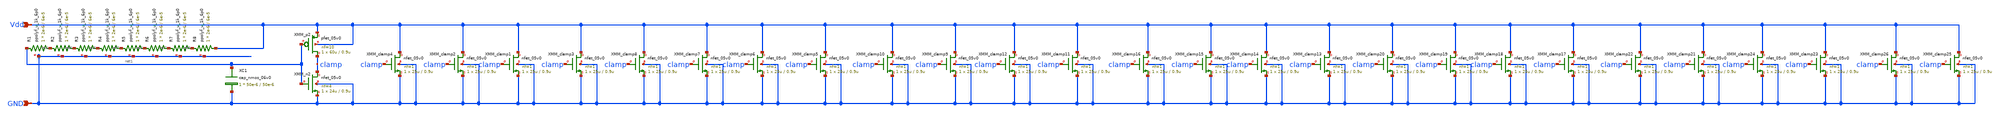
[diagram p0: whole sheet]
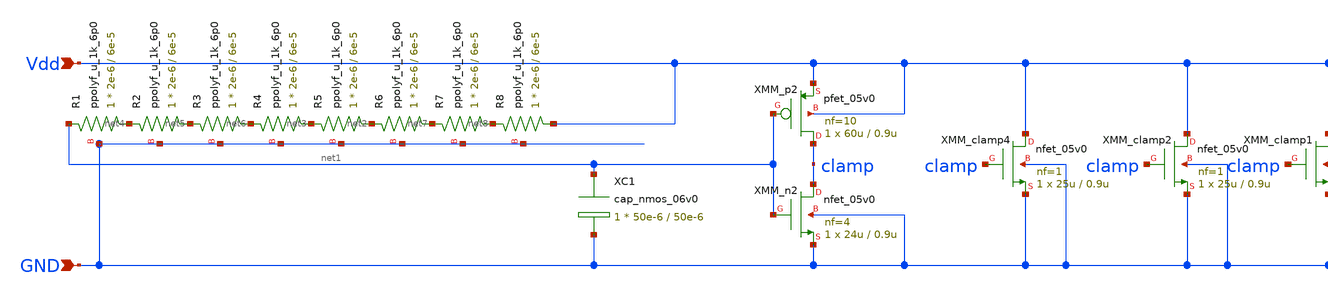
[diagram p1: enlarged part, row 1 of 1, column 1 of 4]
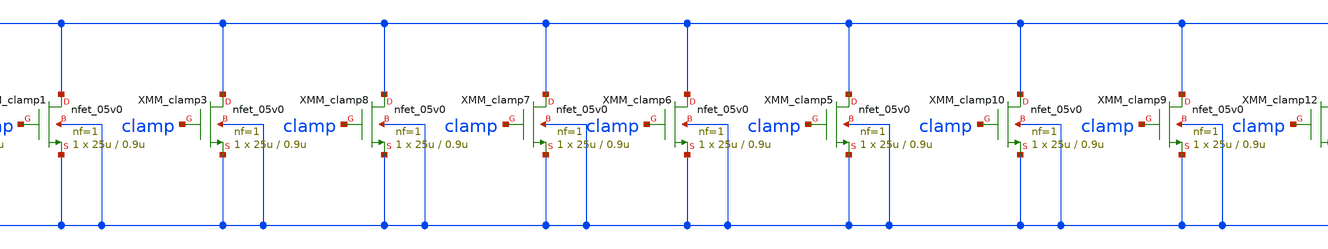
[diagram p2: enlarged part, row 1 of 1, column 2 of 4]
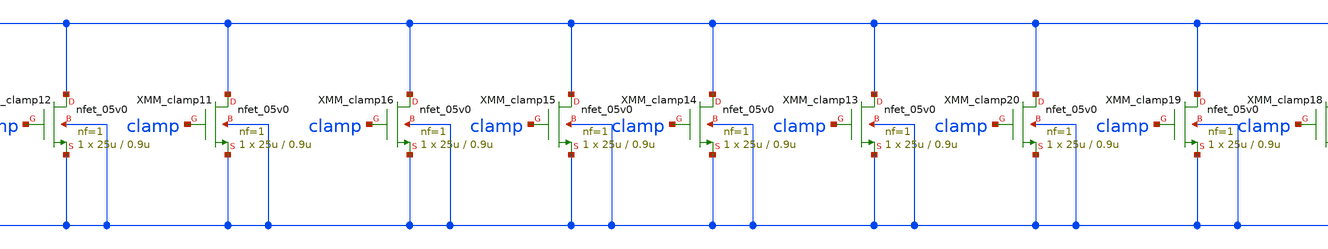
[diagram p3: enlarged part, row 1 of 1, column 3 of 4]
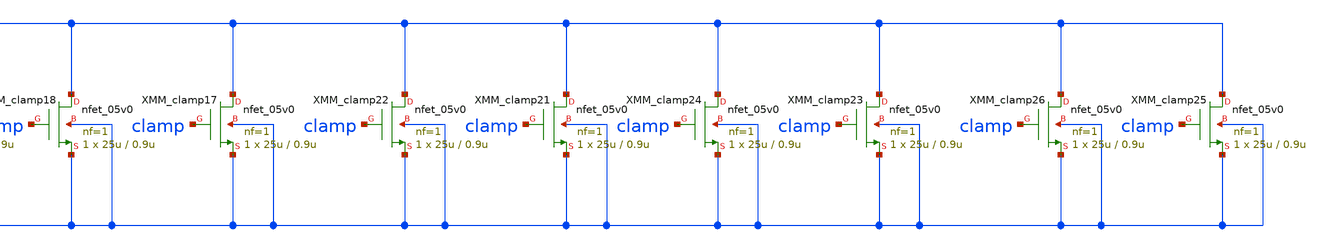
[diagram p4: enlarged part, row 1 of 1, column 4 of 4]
** sch_path: MG_ESD_protection/MG_power_clamp_ESD.sch
**.subckt MG_power_clamp_ESD Vdd GND
*.ipin Vdd
*.ipin GND
XC1 net1 GND cap_nmos_06v0 c_width=50e-6 c_length=50e-6 m=1
XMM_clamp3 Vdd clamp GND GND nfet_05v0 L=0.9u W=25u nf=1 ad='int((nf+1)/2) * W/nf * 0.18u' as='int((nf+2)/2) * W/nf * 0.18u'
+ pd='2*int((nf+1)/2) * (W/nf + 0.18u)' ps='2*int((nf+2)/2) * (W/nf + 0.18u)' nrd='0.18u / W' nrs='0.18u / W'
+ sa=0 sb=0 sd=0 m=1
XMM_clamp1 Vdd clamp GND GND nfet_05v0 L=0.9u W=25u nf=1 ad='int((nf+1)/2) * W/nf * 0.18u' as='int((nf+2)/2) * W/nf * 0.18u'
+ pd='2*int((nf+1)/2) * (W/nf + 0.18u)' ps='2*int((nf+2)/2) * (W/nf + 0.18u)' nrd='0.18u / W' nrs='0.18u / W'
+ sa=0 sb=0 sd=0 m=1
XMM_clamp2 Vdd clamp GND GND nfet_05v0 L=0.9u W=25u nf=1 ad='int((nf+1)/2) * W/nf * 0.18u' as='int((nf+2)/2) * W/nf * 0.18u'
+ pd='2*int((nf+1)/2) * (W/nf + 0.18u)' ps='2*int((nf+2)/2) * (W/nf + 0.18u)' nrd='0.18u / W' nrs='0.18u / W'
+ sa=0 sb=0 sd=0 m=1
XMM_clamp4 Vdd clamp GND GND nfet_05v0 L=0.9u W=25u nf=1 ad='int((nf+1)/2) * W/nf * 0.18u' as='int((nf+2)/2) * W/nf * 0.18u'
+ pd='2*int((nf+1)/2) * (W/nf + 0.18u)' ps='2*int((nf+2)/2) * (W/nf + 0.18u)' nrd='0.18u / W' nrs='0.18u / W'
+ sa=0 sb=0 sd=0 m=1
XMM_clamp5 Vdd clamp GND GND nfet_05v0 L=0.9u W=25u nf=1 ad='int((nf+1)/2) * W/nf * 0.18u' as='int((nf+2)/2) * W/nf * 0.18u'
+ pd='2*int((nf+1)/2) * (W/nf + 0.18u)' ps='2*int((nf+2)/2) * (W/nf + 0.18u)' nrd='0.18u / W' nrs='0.18u / W'
+ sa=0 sb=0 sd=0 m=1
XMM_clamp6 Vdd clamp GND GND nfet_05v0 L=0.9u W=25u nf=1 ad='int((nf+1)/2) * W/nf * 0.18u' as='int((nf+2)/2) * W/nf * 0.18u'
+ pd='2*int((nf+1)/2) * (W/nf + 0.18u)' ps='2*int((nf+2)/2) * (W/nf + 0.18u)' nrd='0.18u / W' nrs='0.18u / W'
+ sa=0 sb=0 sd=0 m=1
XMM_clamp7 Vdd clamp GND GND nfet_05v0 L=0.9u W=25u nf=1 ad='int((nf+1)/2) * W/nf * 0.18u' as='int((nf+2)/2) * W/nf * 0.18u'
+ pd='2*int((nf+1)/2) * (W/nf + 0.18u)' ps='2*int((nf+2)/2) * (W/nf + 0.18u)' nrd='0.18u / W' nrs='0.18u / W'
+ sa=0 sb=0 sd=0 m=1
XMM_clamp8 Vdd clamp GND GND nfet_05v0 L=0.9u W=25u nf=1 ad='int((nf+1)/2) * W/nf * 0.18u' as='int((nf+2)/2) * W/nf * 0.18u'
+ pd='2*int((nf+1)/2) * (W/nf + 0.18u)' ps='2*int((nf+2)/2) * (W/nf + 0.18u)' nrd='0.18u / W' nrs='0.18u / W'
+ sa=0 sb=0 sd=0 m=1
XMM_clamp9 Vdd clamp GND GND nfet_05v0 L=0.9u W=25u nf=1 ad='int((nf+1)/2) * W/nf * 0.18u' as='int((nf+2)/2) * W/nf * 0.18u'
+ pd='2*int((nf+1)/2) * (W/nf + 0.18u)' ps='2*int((nf+2)/2) * (W/nf + 0.18u)' nrd='0.18u / W' nrs='0.18u / W'
+ sa=0 sb=0 sd=0 m=1
XMM_clamp10 Vdd clamp GND GND nfet_05v0 L=0.9u W=25u nf=1 ad='int((nf+1)/2) * W/nf * 0.18u' as='int((nf+2)/2) * W/nf * 0.18u'
+ pd='2*int((nf+1)/2) * (W/nf + 0.18u)' ps='2*int((nf+2)/2) * (W/nf + 0.18u)' nrd='0.18u / W' nrs='0.18u / W'
+ sa=0 sb=0 sd=0 m=1
XMM_clamp11 Vdd clamp GND GND nfet_05v0 L=0.9u W=25u nf=1 ad='int((nf+1)/2) * W/nf * 0.18u' as='int((nf+2)/2) * W/nf * 0.18u'
+ pd='2*int((nf+1)/2) * (W/nf + 0.18u)' ps='2*int((nf+2)/2) * (W/nf + 0.18u)' nrd='0.18u / W' nrs='0.18u / W'
+ sa=0 sb=0 sd=0 m=1
XMM_clamp12 Vdd clamp GND GND nfet_05v0 L=0.9u W=25u nf=1 ad='int((nf+1)/2) * W/nf * 0.18u' as='int((nf+2)/2) * W/nf * 0.18u'
+ pd='2*int((nf+1)/2) * (W/nf + 0.18u)' ps='2*int((nf+2)/2) * (W/nf + 0.18u)' nrd='0.18u / W' nrs='0.18u / W'
+ sa=0 sb=0 sd=0 m=1
XR5 net2 net3 GND ppolyf_u_1k_6p0 r_width=2e-6 r_length=6e-5 m=1
XMM_clamp13 Vdd clamp GND GND nfet_05v0 L=0.9u W=25u nf=1 ad='int((nf+1)/2) * W/nf * 0.18u' as='int((nf+2)/2) * W/nf * 0.18u'
+ pd='2*int((nf+1)/2) * (W/nf + 0.18u)' ps='2*int((nf+2)/2) * (W/nf + 0.18u)' nrd='0.18u / W' nrs='0.18u / W'
+ sa=0 sb=0 sd=0 m=1
XMM_clamp14 Vdd clamp GND GND nfet_05v0 L=0.9u W=25u nf=1 ad='int((nf+1)/2) * W/nf * 0.18u' as='int((nf+2)/2) * W/nf * 0.18u'
+ pd='2*int((nf+1)/2) * (W/nf + 0.18u)' ps='2*int((nf+2)/2) * (W/nf + 0.18u)' nrd='0.18u / W' nrs='0.18u / W'
+ sa=0 sb=0 sd=0 m=1
XMM_clamp15 Vdd clamp GND GND nfet_05v0 L=0.9u W=25u nf=1 ad='int((nf+1)/2) * W/nf * 0.18u' as='int((nf+2)/2) * W/nf * 0.18u'
+ pd='2*int((nf+1)/2) * (W/nf + 0.18u)' ps='2*int((nf+2)/2) * (W/nf + 0.18u)' nrd='0.18u / W' nrs='0.18u / W'
+ sa=0 sb=0 sd=0 m=1
XMM_clamp16 Vdd clamp GND GND nfet_05v0 L=0.9u W=25u nf=1 ad='int((nf+1)/2) * W/nf * 0.18u' as='int((nf+2)/2) * W/nf * 0.18u'
+ pd='2*int((nf+1)/2) * (W/nf + 0.18u)' ps='2*int((nf+2)/2) * (W/nf + 0.18u)' nrd='0.18u / W' nrs='0.18u / W'
+ sa=0 sb=0 sd=0 m=1
XMM_clamp17 Vdd clamp GND GND nfet_05v0 L=0.9u W=25u nf=1 ad='int((nf+1)/2) * W/nf * 0.18u' as='int((nf+2)/2) * W/nf * 0.18u'
+ pd='2*int((nf+1)/2) * (W/nf + 0.18u)' ps='2*int((nf+2)/2) * (W/nf + 0.18u)' nrd='0.18u / W' nrs='0.18u / W'
+ sa=0 sb=0 sd=0 m=1
XMM_clamp18 Vdd clamp GND GND nfet_05v0 L=0.9u W=25u nf=1 ad='int((nf+1)/2) * W/nf * 0.18u' as='int((nf+2)/2) * W/nf * 0.18u'
+ pd='2*int((nf+1)/2) * (W/nf + 0.18u)' ps='2*int((nf+2)/2) * (W/nf + 0.18u)' nrd='0.18u / W' nrs='0.18u / W'
+ sa=0 sb=0 sd=0 m=1
XMM_clamp19 Vdd clamp GND GND nfet_05v0 L=0.9u W=25u nf=1 ad='int((nf+1)/2) * W/nf * 0.18u' as='int((nf+2)/2) * W/nf * 0.18u'
+ pd='2*int((nf+1)/2) * (W/nf + 0.18u)' ps='2*int((nf+2)/2) * (W/nf + 0.18u)' nrd='0.18u / W' nrs='0.18u / W'
+ sa=0 sb=0 sd=0 m=1
XMM_clamp20 Vdd clamp GND GND nfet_05v0 L=0.9u W=25u nf=1 ad='int((nf+1)/2) * W/nf * 0.18u' as='int((nf+2)/2) * W/nf * 0.18u'
+ pd='2*int((nf+1)/2) * (W/nf + 0.18u)' ps='2*int((nf+2)/2) * (W/nf + 0.18u)' nrd='0.18u / W' nrs='0.18u / W'
+ sa=0 sb=0 sd=0 m=1
XMM_clamp21 Vdd clamp GND GND nfet_05v0 L=0.9u W=25u nf=1 ad='int((nf+1)/2) * W/nf * 0.18u' as='int((nf+2)/2) * W/nf * 0.18u'
+ pd='2*int((nf+1)/2) * (W/nf + 0.18u)' ps='2*int((nf+2)/2) * (W/nf + 0.18u)' nrd='0.18u / W' nrs='0.18u / W'
+ sa=0 sb=0 sd=0 m=1
XMM_clamp22 Vdd clamp GND GND nfet_05v0 L=0.9u W=25u nf=1 ad='int((nf+1)/2) * W/nf * 0.18u' as='int((nf+2)/2) * W/nf * 0.18u'
+ pd='2*int((nf+1)/2) * (W/nf + 0.18u)' ps='2*int((nf+2)/2) * (W/nf + 0.18u)' nrd='0.18u / W' nrs='0.18u / W'
+ sa=0 sb=0 sd=0 m=1
XMM_clamp23 Vdd clamp GND GND nfet_05v0 L=0.9u W=25u nf=1 ad='int((nf+1)/2) * W/nf * 0.18u' as='int((nf+2)/2) * W/nf * 0.18u'
+ pd='2*int((nf+1)/2) * (W/nf + 0.18u)' ps='2*int((nf+2)/2) * (W/nf + 0.18u)' nrd='0.18u / W' nrs='0.18u / W'
+ sa=0 sb=0 sd=0 m=1
XMM_clamp24 Vdd clamp GND GND nfet_05v0 L=0.9u W=25u nf=1 ad='int((nf+1)/2) * W/nf * 0.18u' as='int((nf+2)/2) * W/nf * 0.18u'
+ pd='2*int((nf+1)/2) * (W/nf + 0.18u)' ps='2*int((nf+2)/2) * (W/nf + 0.18u)' nrd='0.18u / W' nrs='0.18u / W'
+ sa=0 sb=0 sd=0 m=1
XMM_p2 clamp net1 Vdd Vdd pfet_05v0 L=0.9u W=60u nf=10 ad='int((nf+1)/2) * W/nf * 0.18u' as='int((nf+2)/2) * W/nf * 0.18u'
+ pd='2*int((nf+1)/2) * (W/nf + 0.18u)' ps='2*int((nf+2)/2) * (W/nf + 0.18u)' nrd='0.18u / W' nrs='0.18u / W'
+ sa=0 sb=0 sd=0 m=1
XMM_n2 clamp net1 GND GND nfet_05v0 L=0.9u W=24u nf=4 ad='int((nf+1)/2) * W/nf * 0.18u' as='int((nf+2)/2) * W/nf * 0.18u'
+ pd='2*int((nf+1)/2) * (W/nf + 0.18u)' ps='2*int((nf+2)/2) * (W/nf + 0.18u)' nrd='0.18u / W' nrs='0.18u / W'
+ sa=0 sb=0 sd=0 m=1
XR1 net4 net1 GND ppolyf_u_1k_6p0 r_width=2e-6 r_length=6e-5 m=1
XR2 net5 net4 GND ppolyf_u_1k_6p0 r_width=2e-6 r_length=6e-5 m=1
XR3 net6 net5 GND ppolyf_u_1k_6p0 r_width=2e-6 r_length=6e-5 m=1
XR4 net3 net6 GND ppolyf_u_1k_6p0 r_width=2e-6 r_length=6e-5 m=1
XR6 net7 net2 GND ppolyf_u_1k_6p0 r_width=2e-6 r_length=6e-5 m=1
XR7 net8 net7 GND ppolyf_u_1k_6p0 r_width=2e-6 r_length=6e-5 m=1
XR8 Vdd net8 GND ppolyf_u_1k_6p0 r_width=2e-6 r_length=6e-5 m=1
XMM_clamp25 Vdd clamp GND GND nfet_05v0 L=0.9u W=25u nf=1 ad='int((nf+1)/2) * W/nf * 0.18u' as='int((nf+2)/2) * W/nf * 0.18u'
+ pd='2*int((nf+1)/2) * (W/nf + 0.18u)' ps='2*int((nf+2)/2) * (W/nf + 0.18u)' nrd='0.18u / W' nrs='0.18u / W'
+ sa=0 sb=0 sd=0 m=1
XMM_clamp26 Vdd clamp GND GND nfet_05v0 L=0.9u W=25u nf=1 ad='int((nf+1)/2) * W/nf * 0.18u' as='int((nf+2)/2) * W/nf * 0.18u'
+ pd='2*int((nf+1)/2) * (W/nf + 0.18u)' ps='2*int((nf+2)/2) * (W/nf + 0.18u)' nrd='0.18u / W' nrs='0.18u / W'
+ sa=0 sb=0 sd=0 m=1
**.ends
.end
